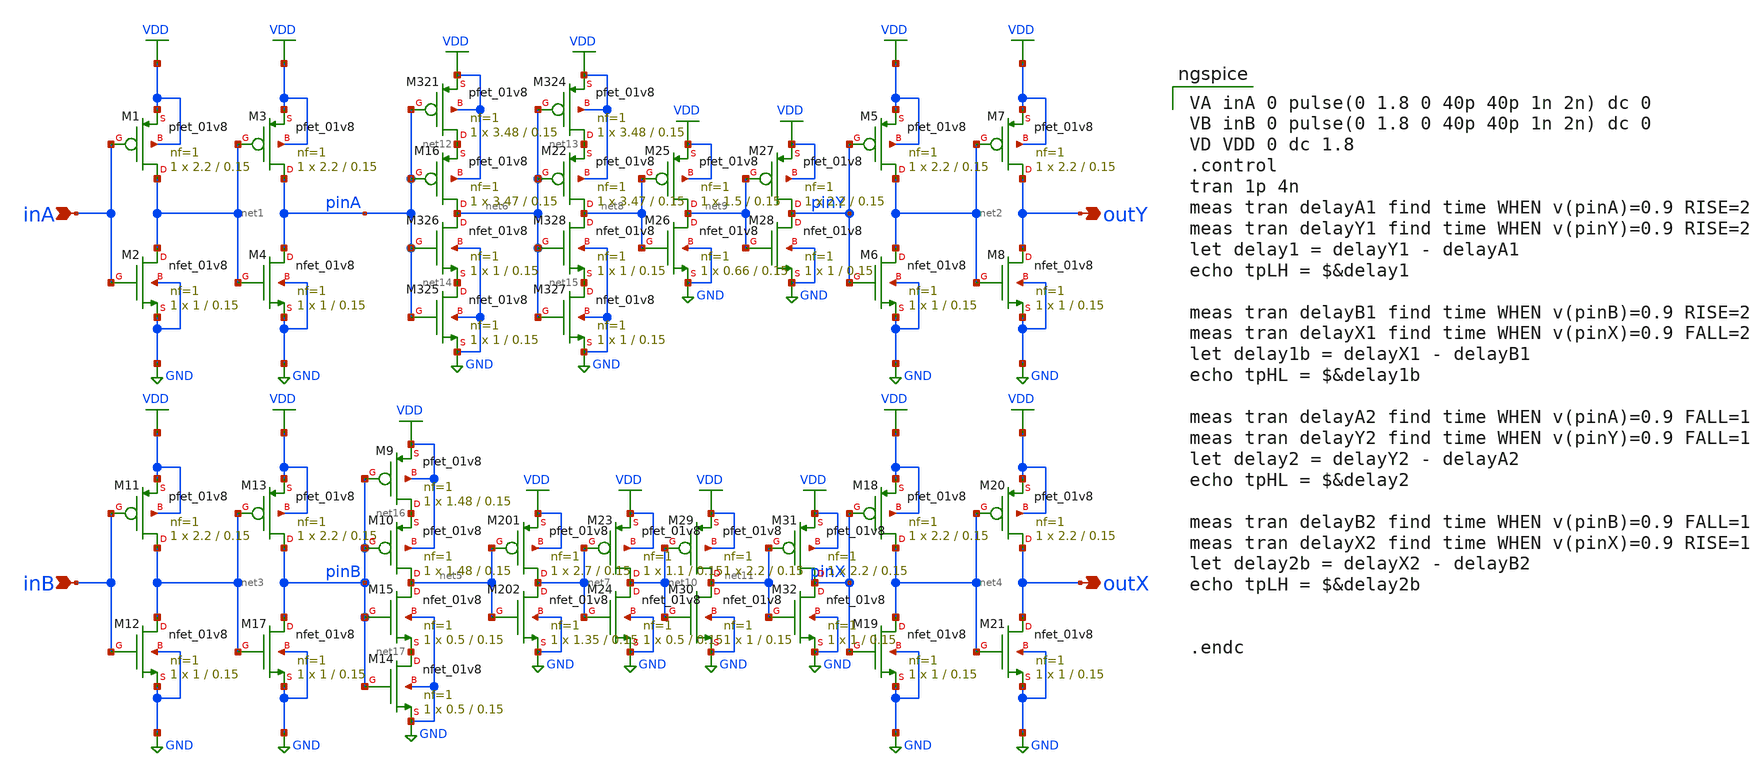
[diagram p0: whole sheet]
** sch_path: inv_meas2.sch
**.subckt inv_meas2 inA outY inB outX
*.ipin inA
*.opin outY
*.ipin inB
*.opin outX
XM1 net1 inA VDD VDD sky130_fd_pr__pfet_01v8 L=0.15 W=2.2 nf=1 ad='int((nf+1)/2) * W/nf * 0.29' as='int((nf+2)/2) * W/nf * 0.29'
+ pd='2*int((nf+1)/2) * (W/nf + 0.29)' ps='2*int((nf+2)/2) * (W/nf + 0.29)' nrd='0.29 / W' nrs='0.29 / W'
+ sa=0 sb=0 sd=0 mult=1 m=1
XM2 net1 inA GND GND sky130_fd_pr__nfet_01v8 L=0.15 W=1 nf=1 ad='int((nf+1)/2) * W/nf * 0.29' as='int((nf+2)/2) * W/nf * 0.29'
+ pd='2*int((nf+1)/2) * (W/nf + 0.29)' ps='2*int((nf+2)/2) * (W/nf + 0.29)' nrd='0.29 / W' nrs='0.29 / W'
+ sa=0 sb=0 sd=0 mult=1 m=1
XM3 pinA net1 VDD VDD sky130_fd_pr__pfet_01v8 L=0.15 W=2.2 nf=1 ad='int((nf+1)/2) * W/nf * 0.29' as='int((nf+2)/2) * W/nf * 0.29'
+ pd='2*int((nf+1)/2) * (W/nf + 0.29)' ps='2*int((nf+2)/2) * (W/nf + 0.29)' nrd='0.29 / W' nrs='0.29 / W'
+ sa=0 sb=0 sd=0 mult=1 m=1
XM4 pinA net1 GND GND sky130_fd_pr__nfet_01v8 L=0.15 W=1 nf=1 ad='int((nf+1)/2) * W/nf * 0.29' as='int((nf+2)/2) * W/nf * 0.29'
+ pd='2*int((nf+1)/2) * (W/nf + 0.29)' ps='2*int((nf+2)/2) * (W/nf + 0.29)' nrd='0.29 / W' nrs='0.29 / W'
+ sa=0 sb=0 sd=0 mult=1 m=1
XM5 net2 pinY VDD VDD sky130_fd_pr__pfet_01v8 L=0.15 W=2.2 nf=1 ad='int((nf+1)/2) * W/nf * 0.29' as='int((nf+2)/2) * W/nf * 0.29'
+ pd='2*int((nf+1)/2) * (W/nf + 0.29)' ps='2*int((nf+2)/2) * (W/nf + 0.29)' nrd='0.29 / W' nrs='0.29 / W'
+ sa=0 sb=0 sd=0 mult=1 m=1
XM6 net2 pinY GND GND sky130_fd_pr__nfet_01v8 L=0.15 W=1 nf=1 ad='int((nf+1)/2) * W/nf * 0.29' as='int((nf+2)/2) * W/nf * 0.29'
+ pd='2*int((nf+1)/2) * (W/nf + 0.29)' ps='2*int((nf+2)/2) * (W/nf + 0.29)' nrd='0.29 / W' nrs='0.29 / W'
+ sa=0 sb=0 sd=0 mult=1 m=1
XM7 outY net2 VDD VDD sky130_fd_pr__pfet_01v8 L=0.15 W=2.2 nf=1 ad='int((nf+1)/2) * W/nf * 0.29' as='int((nf+2)/2) * W/nf * 0.29'
+ pd='2*int((nf+1)/2) * (W/nf + 0.29)' ps='2*int((nf+2)/2) * (W/nf + 0.29)' nrd='0.29 / W' nrs='0.29 / W'
+ sa=0 sb=0 sd=0 mult=1 m=1
XM8 outY net2 GND GND sky130_fd_pr__nfet_01v8 L=0.15 W=1 nf=1 ad='int((nf+1)/2) * W/nf * 0.29' as='int((nf+2)/2) * W/nf * 0.29'
+ pd='2*int((nf+1)/2) * (W/nf + 0.29)' ps='2*int((nf+2)/2) * (W/nf + 0.29)' nrd='0.29 / W' nrs='0.29 / W'
+ sa=0 sb=0 sd=0 mult=1 m=1
XM11 net3 inB VDD VDD sky130_fd_pr__pfet_01v8 L=0.15 W=2.2 nf=1 ad='int((nf+1)/2) * W/nf * 0.29' as='int((nf+2)/2) * W/nf * 0.29'
+ pd='2*int((nf+1)/2) * (W/nf + 0.29)' ps='2*int((nf+2)/2) * (W/nf + 0.29)' nrd='0.29 / W' nrs='0.29 / W'
+ sa=0 sb=0 sd=0 mult=1 m=1
XM12 net3 inB GND GND sky130_fd_pr__nfet_01v8 L=0.15 W=1 nf=1 ad='int((nf+1)/2) * W/nf * 0.29' as='int((nf+2)/2) * W/nf * 0.29'
+ pd='2*int((nf+1)/2) * (W/nf + 0.29)' ps='2*int((nf+2)/2) * (W/nf + 0.29)' nrd='0.29 / W' nrs='0.29 / W'
+ sa=0 sb=0 sd=0 mult=1 m=1
XM13 pinB net3 VDD VDD sky130_fd_pr__pfet_01v8 L=0.15 W=2.2 nf=1 ad='int((nf+1)/2) * W/nf * 0.29' as='int((nf+2)/2) * W/nf * 0.29'
+ pd='2*int((nf+1)/2) * (W/nf + 0.29)' ps='2*int((nf+2)/2) * (W/nf + 0.29)' nrd='0.29 / W' nrs='0.29 / W'
+ sa=0 sb=0 sd=0 mult=1 m=1
XM17 pinB net3 GND GND sky130_fd_pr__nfet_01v8 L=0.15 W=1 nf=1 ad='int((nf+1)/2) * W/nf * 0.29' as='int((nf+2)/2) * W/nf * 0.29'
+ pd='2*int((nf+1)/2) * (W/nf + 0.29)' ps='2*int((nf+2)/2) * (W/nf + 0.29)' nrd='0.29 / W' nrs='0.29 / W'
+ sa=0 sb=0 sd=0 mult=1 m=1
XM18 net4 pinX VDD VDD sky130_fd_pr__pfet_01v8 L=0.15 W=2.2 nf=1 ad='int((nf+1)/2) * W/nf * 0.29' as='int((nf+2)/2) * W/nf * 0.29'
+ pd='2*int((nf+1)/2) * (W/nf + 0.29)' ps='2*int((nf+2)/2) * (W/nf + 0.29)' nrd='0.29 / W' nrs='0.29 / W'
+ sa=0 sb=0 sd=0 mult=1 m=1
XM19 net4 pinX GND GND sky130_fd_pr__nfet_01v8 L=0.15 W=1 nf=1 ad='int((nf+1)/2) * W/nf * 0.29' as='int((nf+2)/2) * W/nf * 0.29'
+ pd='2*int((nf+1)/2) * (W/nf + 0.29)' ps='2*int((nf+2)/2) * (W/nf + 0.29)' nrd='0.29 / W' nrs='0.29 / W'
+ sa=0 sb=0 sd=0 mult=1 m=1
XM20 outX net4 VDD VDD sky130_fd_pr__pfet_01v8 L=0.15 W=2.2 nf=1 ad='int((nf+1)/2) * W/nf * 0.29' as='int((nf+2)/2) * W/nf * 0.29'
+ pd='2*int((nf+1)/2) * (W/nf + 0.29)' ps='2*int((nf+2)/2) * (W/nf + 0.29)' nrd='0.29 / W' nrs='0.29 / W'
+ sa=0 sb=0 sd=0 mult=1 m=1
XM21 outX net4 GND GND sky130_fd_pr__nfet_01v8 L=0.15 W=1 nf=1 ad='int((nf+1)/2) * W/nf * 0.29' as='int((nf+2)/2) * W/nf * 0.29'
+ pd='2*int((nf+1)/2) * (W/nf + 0.29)' ps='2*int((nf+2)/2) * (W/nf + 0.29)' nrd='0.29 / W' nrs='0.29 / W'
+ sa=0 sb=0 sd=0 mult=1 m=1
XM321 net12 pinA VDD VDD sky130_fd_pr__pfet_01v8 L=0.15 W=3.48 nf=1 ad='int((nf+1)/2) * W/nf * 0.29'
+ as='int((nf+2)/2) * W/nf * 0.29' pd='2*int((nf+1)/2) * (W/nf + 0.29)' ps='2*int((nf+2)/2) * (W/nf + 0.29)'
+ nrd='0.29 / W' nrs='0.29 / W' sa=0 sb=0 sd=0 mult=1 m=1
XM324 net13 net6 VDD VDD sky130_fd_pr__pfet_01v8 L=0.15 W=3.48 nf=1 ad='int((nf+1)/2) * W/nf * 0.29'
+ as='int((nf+2)/2) * W/nf * 0.29' pd='2*int((nf+1)/2) * (W/nf + 0.29)' ps='2*int((nf+2)/2) * (W/nf + 0.29)'
+ nrd='0.29 / W' nrs='0.29 / W' sa=0 sb=0 sd=0 mult=1 m=1
XM325 net14 pinA GND GND sky130_fd_pr__nfet_01v8 L=0.15 W=1 nf=1 ad='int((nf+1)/2) * W/nf * 0.29' as='int((nf+2)/2) * W/nf * 0.29'
+ pd='2*int((nf+1)/2) * (W/nf + 0.29)' ps='2*int((nf+2)/2) * (W/nf + 0.29)' nrd='0.29 / W' nrs='0.29 / W'
+ sa=0 sb=0 sd=0 mult=1 m=1
XM326 net6 pinA net14 GND sky130_fd_pr__nfet_01v8 L=0.15 W=1 nf=1 ad='int((nf+1)/2) * W/nf * 0.29' as='int((nf+2)/2) * W/nf * 0.29'
+ pd='2*int((nf+1)/2) * (W/nf + 0.29)' ps='2*int((nf+2)/2) * (W/nf + 0.29)' nrd='0.29 / W' nrs='0.29 / W'
+ sa=0 sb=0 sd=0 mult=1 m=1
XM327 net15 net6 GND GND sky130_fd_pr__nfet_01v8 L=0.15 W=1 nf=1 ad='int((nf+1)/2) * W/nf * 0.29' as='int((nf+2)/2) * W/nf * 0.29'
+ pd='2*int((nf+1)/2) * (W/nf + 0.29)' ps='2*int((nf+2)/2) * (W/nf + 0.29)' nrd='0.29 / W' nrs='0.29 / W'
+ sa=0 sb=0 sd=0 mult=1 m=1
XM328 net8 net6 net15 GND sky130_fd_pr__nfet_01v8 L=0.15 W=1 nf=1 ad='int((nf+1)/2) * W/nf * 0.29' as='int((nf+2)/2) * W/nf * 0.29'
+ pd='2*int((nf+1)/2) * (W/nf + 0.29)' ps='2*int((nf+2)/2) * (W/nf + 0.29)' nrd='0.29 / W' nrs='0.29 / W'
+ sa=0 sb=0 sd=0 mult=1 m=1
XM9 net16 pinB VDD VDD sky130_fd_pr__pfet_01v8 L=0.15 W=1.48 nf=1 ad='int((nf+1)/2) * W/nf * 0.29' as='int((nf+2)/2) * W/nf * 0.29'
+ pd='2*int((nf+1)/2) * (W/nf + 0.29)' ps='2*int((nf+2)/2) * (W/nf + 0.29)' nrd='0.29 / W' nrs='0.29 / W'
+ sa=0 sb=0 sd=0 mult=1 m=1
XM10 net5 pinB net16 VDD sky130_fd_pr__pfet_01v8 L=0.15 W=1.48 nf=1 ad='int((nf+1)/2) * W/nf * 0.29'
+ as='int((nf+2)/2) * W/nf * 0.29' pd='2*int((nf+1)/2) * (W/nf + 0.29)' ps='2*int((nf+2)/2) * (W/nf + 0.29)'
+ nrd='0.29 / W' nrs='0.29 / W' sa=0 sb=0 sd=0 mult=1 m=1
XM14 net17 pinB GND GND sky130_fd_pr__nfet_01v8 L=0.15 W=0.5 nf=1 ad='int((nf+1)/2) * W/nf * 0.29' as='int((nf+2)/2) * W/nf * 0.29'
+ pd='2*int((nf+1)/2) * (W/nf + 0.29)' ps='2*int((nf+2)/2) * (W/nf + 0.29)' nrd='0.29 / W' nrs='0.29 / W'
+ sa=0 sb=0 sd=0 mult=1 m=1
XM15 net5 pinB net17 GND sky130_fd_pr__nfet_01v8 L=0.15 W=0.5 nf=1 ad='int((nf+1)/2) * W/nf * 0.29' as='int((nf+2)/2) * W/nf * 0.29'
+ pd='2*int((nf+1)/2) * (W/nf + 0.29)' ps='2*int((nf+2)/2) * (W/nf + 0.29)' nrd='0.29 / W' nrs='0.29 / W'
+ sa=0 sb=0 sd=0 mult=1 m=1
XM16 net6 pinA net12 VDD sky130_fd_pr__pfet_01v8 L=0.15 W=3.47 nf=1 ad='int((nf+1)/2) * W/nf * 0.29'
+ as='int((nf+2)/2) * W/nf * 0.29' pd='2*int((nf+1)/2) * (W/nf + 0.29)' ps='2*int((nf+2)/2) * (W/nf + 0.29)'
+ nrd='0.29 / W' nrs='0.29 / W' sa=0 sb=0 sd=0 mult=1 m=1
XM22 net8 net6 net13 VDD sky130_fd_pr__pfet_01v8 L=0.15 W=3.47 nf=1 ad='int((nf+1)/2) * W/nf * 0.29'
+ as='int((nf+2)/2) * W/nf * 0.29' pd='2*int((nf+1)/2) * (W/nf + 0.29)' ps='2*int((nf+2)/2) * (W/nf + 0.29)'
+ nrd='0.29 / W' nrs='0.29 / W' sa=0 sb=0 sd=0 mult=1 m=1
XM201 net7 net5 VDD VDD sky130_fd_pr__pfet_01v8 L=0.15 W=2.7 nf=1 ad='int((nf+1)/2) * W/nf * 0.29' as='int((nf+2)/2) * W/nf * 0.29'
+ pd='2*int((nf+1)/2) * (W/nf + 0.29)' ps='2*int((nf+2)/2) * (W/nf + 0.29)' nrd='0.29 / W' nrs='0.29 / W'
+ sa=0 sb=0 sd=0 mult=1 m=1
XM202 net7 net5 GND GND sky130_fd_pr__nfet_01v8 L=0.15 W=1.35 nf=1 ad='int((nf+1)/2) * W/nf * 0.29' as='int((nf+2)/2) * W/nf * 0.29'
+ pd='2*int((nf+1)/2) * (W/nf + 0.29)' ps='2*int((nf+2)/2) * (W/nf + 0.29)' nrd='0.29 / W' nrs='0.29 / W'
+ sa=0 sb=0 sd=0 mult=1 m=1
XM23 net10 net7 VDD VDD sky130_fd_pr__pfet_01v8 L=0.15 W=1.1 nf=1 ad='int((nf+1)/2) * W/nf * 0.29' as='int((nf+2)/2) * W/nf * 0.29'
+ pd='2*int((nf+1)/2) * (W/nf + 0.29)' ps='2*int((nf+2)/2) * (W/nf + 0.29)' nrd='0.29 / W' nrs='0.29 / W'
+ sa=0 sb=0 sd=0 mult=1 m=1
XM24 net10 net7 GND GND sky130_fd_pr__nfet_01v8 L=0.15 W=0.5 nf=1 ad='int((nf+1)/2) * W/nf * 0.29' as='int((nf+2)/2) * W/nf * 0.29'
+ pd='2*int((nf+1)/2) * (W/nf + 0.29)' ps='2*int((nf+2)/2) * (W/nf + 0.29)' nrd='0.29 / W' nrs='0.29 / W'
+ sa=0 sb=0 sd=0 mult=1 m=1
XM25 net9 net8 VDD VDD sky130_fd_pr__pfet_01v8 L=0.15 W=1.5 nf=1 ad='int((nf+1)/2) * W/nf * 0.29' as='int((nf+2)/2) * W/nf * 0.29'
+ pd='2*int((nf+1)/2) * (W/nf + 0.29)' ps='2*int((nf+2)/2) * (W/nf + 0.29)' nrd='0.29 / W' nrs='0.29 / W'
+ sa=0 sb=0 sd=0 mult=1 m=1
XM26 net9 net8 GND GND sky130_fd_pr__nfet_01v8 L=0.15 W=0.66 nf=1 ad='int((nf+1)/2) * W/nf * 0.29' as='int((nf+2)/2) * W/nf * 0.29'
+ pd='2*int((nf+1)/2) * (W/nf + 0.29)' ps='2*int((nf+2)/2) * (W/nf + 0.29)' nrd='0.29 / W' nrs='0.29 / W'
+ sa=0 sb=0 sd=0 mult=1 m=1
XM27 pinY net9 VDD VDD sky130_fd_pr__pfet_01v8 L=0.15 W=2.2 nf=1 ad='int((nf+1)/2) * W/nf * 0.29' as='int((nf+2)/2) * W/nf * 0.29'
+ pd='2*int((nf+1)/2) * (W/nf + 0.29)' ps='2*int((nf+2)/2) * (W/nf + 0.29)' nrd='0.29 / W' nrs='0.29 / W'
+ sa=0 sb=0 sd=0 mult=1 m=1
XM28 pinY net9 GND GND sky130_fd_pr__nfet_01v8 L=0.15 W=1 nf=1 ad='int((nf+1)/2) * W/nf * 0.29' as='int((nf+2)/2) * W/nf * 0.29'
+ pd='2*int((nf+1)/2) * (W/nf + 0.29)' ps='2*int((nf+2)/2) * (W/nf + 0.29)' nrd='0.29 / W' nrs='0.29 / W'
+ sa=0 sb=0 sd=0 mult=1 m=1
XM29 net11 net10 VDD VDD sky130_fd_pr__pfet_01v8 L=0.15 W=2.2 nf=1 ad='int((nf+1)/2) * W/nf * 0.29' as='int((nf+2)/2) * W/nf * 0.29'
+ pd='2*int((nf+1)/2) * (W/nf + 0.29)' ps='2*int((nf+2)/2) * (W/nf + 0.29)' nrd='0.29 / W' nrs='0.29 / W'
+ sa=0 sb=0 sd=0 mult=1 m=1
XM30 net11 net10 GND GND sky130_fd_pr__nfet_01v8 L=0.15 W=1 nf=1 ad='int((nf+1)/2) * W/nf * 0.29' as='int((nf+2)/2) * W/nf * 0.29'
+ pd='2*int((nf+1)/2) * (W/nf + 0.29)' ps='2*int((nf+2)/2) * (W/nf + 0.29)' nrd='0.29 / W' nrs='0.29 / W'
+ sa=0 sb=0 sd=0 mult=1 m=1
XM31 pinX net11 VDD VDD sky130_fd_pr__pfet_01v8 L=0.15 W=2.2 nf=1 ad='int((nf+1)/2) * W/nf * 0.29' as='int((nf+2)/2) * W/nf * 0.29'
+ pd='2*int((nf+1)/2) * (W/nf + 0.29)' ps='2*int((nf+2)/2) * (W/nf + 0.29)' nrd='0.29 / W' nrs='0.29 / W'
+ sa=0 sb=0 sd=0 mult=1 m=1
XM32 pinX net11 GND GND sky130_fd_pr__nfet_01v8 L=0.15 W=1 nf=1 ad='int((nf+1)/2) * W/nf * 0.29' as='int((nf+2)/2) * W/nf * 0.29'
+ pd='2*int((nf+1)/2) * (W/nf + 0.29)' ps='2*int((nf+2)/2) * (W/nf + 0.29)' nrd='0.29 / W' nrs='0.29 / W'
+ sa=0 sb=0 sd=0 mult=1 m=1
**** begin user architecture code

VA inA 0 pulse(0 1.8 0 40p 40p 1n 2n) dc 0
VB inB 0 pulse(0 1.8 0 40p 40p 1n 2n) dc 0
VD VDD 0 dc 1.8
.control
tran 1p 4n
meas tran delayA1 find time WHEN v(pinA)=0.9 RISE=2
meas tran delayY1 find time WHEN v(pinY)=0.9 RISE=2
let delay1 = delayY1 - delayA1
echo tpLH = $&delay1

meas tran delayB1 find time WHEN v(pinB)=0.9 RISE=2
meas tran delayX1 find time WHEN v(pinX)=0.9 FALL=2
let delay1b = delayX1 - delayB1
echo tpHL = $&delay1b

meas tran delayA2 find time WHEN v(pinA)=0.9 FALL=1
meas tran delayY2 find time WHEN v(pinY)=0.9 FALL=1
let delay2 = delayY2 - delayA2
echo tpHL = $&delay2

meas tran delayB2 find time WHEN v(pinB)=0.9 FALL=1
meas tran delayX2 find time WHEN v(pinX)=0.9 RISE=1
let delay2b = delayX2 - delayB2
echo tpLH = $&delay2b


.endc

 .param mc_mm_switch=0
.param mc_pr_switch=0
.include $::SKYWATER_MODELS/corners/tt.spice
.include $::SKYWATER_MODELS/r+c/res_typical__cap_typical.spice
.include $::SKYWATER_MODELS/r+c/res_typical__cap_typical__lin.spice
.include $::SKYWATER_MODELS/corners/tt/specialized_cells.spice
.include $::SKYWATER_STDCELLS/sky130_fd_sc_hd.spice

**** end user architecture code
**.ends
.GLOBAL GND
.GLOBAL VDD
.end
